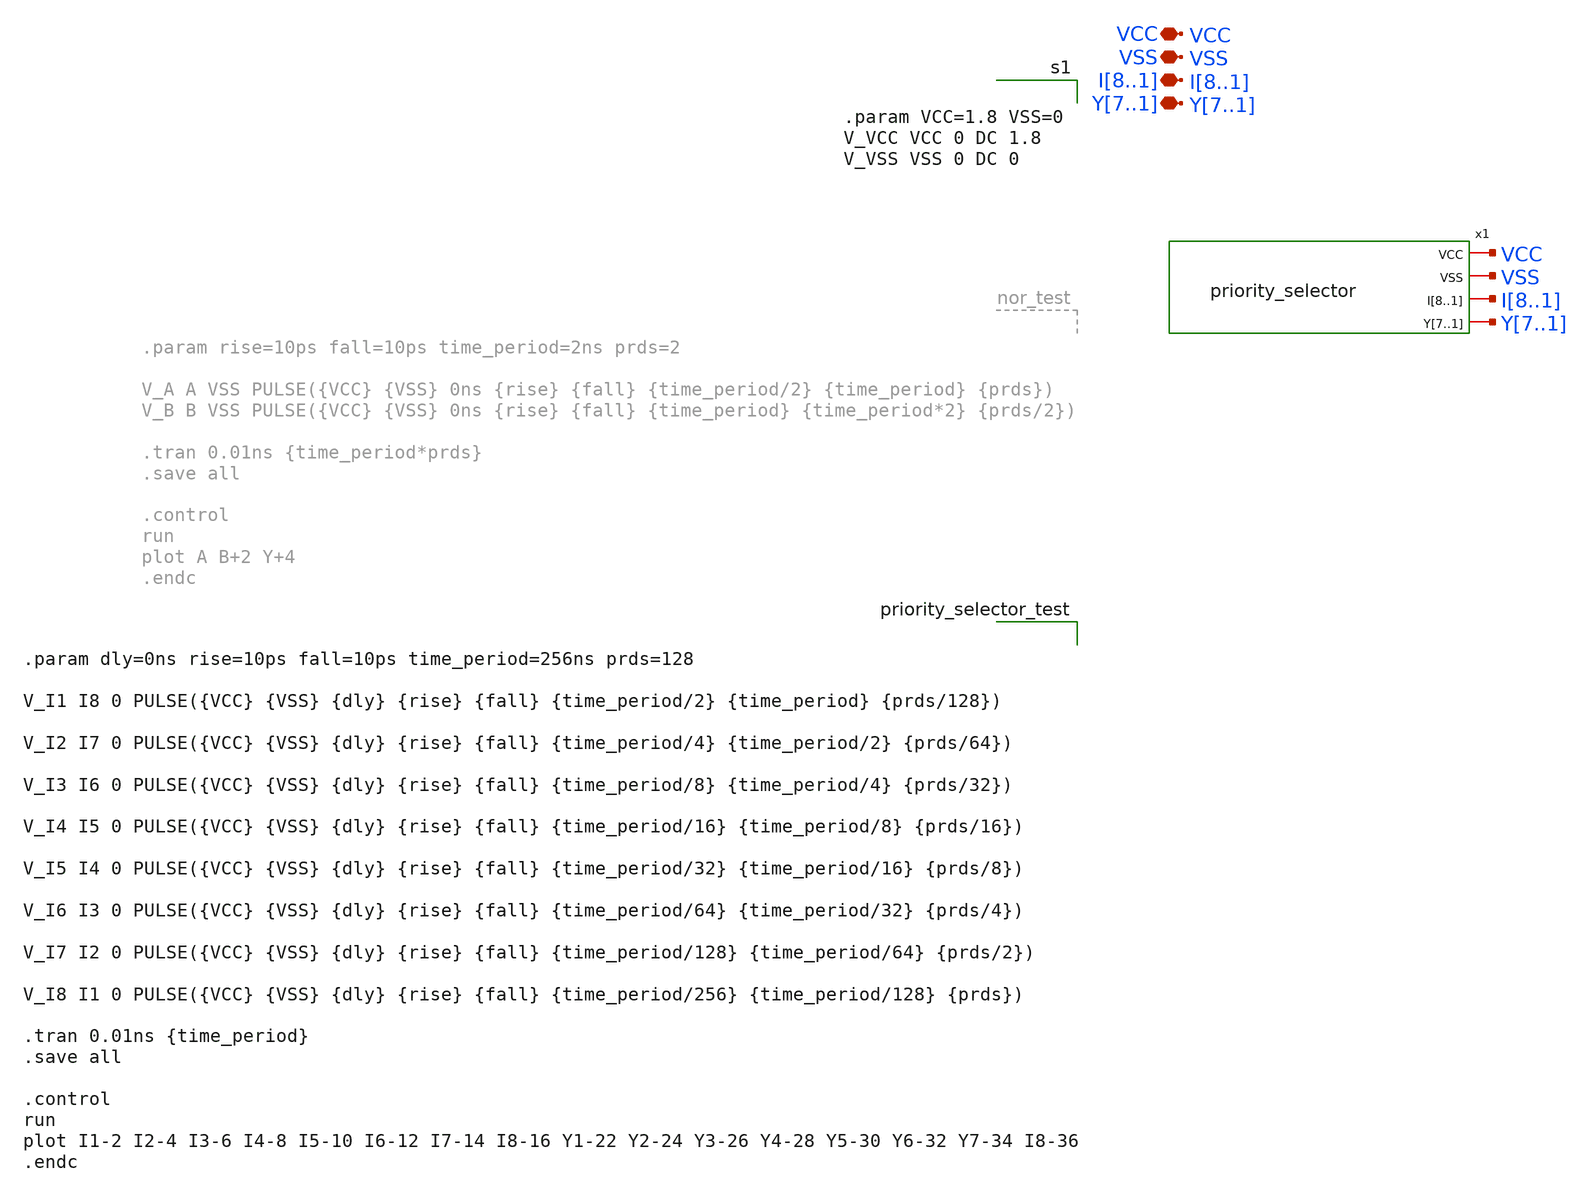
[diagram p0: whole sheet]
** sch_path: peripherals/priority_selector_test.sch
**.subckt priority_selector_test VSS VCC I8,I7,I6,I5,I4,I3,I2,I1 Y7,Y6,Y5,Y4,Y3,Y2,Y1
*.iopin VSS
*.iopin VCC
*.iopin I8,I7,I6,I5,I4,I3,I2,I1
*.iopin Y7,Y6,Y5,Y4,Y3,Y2,Y1
x1 VCC VSS I8 I7 I6 I5 I4 I3 I2 I1 Y7 Y6 Y5 Y4 Y3 Y2 Y1 priority_selector
**** begin user architecture code


.param VCC=1.8 VSS=0
V_VCC VCC 0 DC 1.8
V_VSS VSS 0 DC 0



** opencircuitdesign pdks install
.lib $::SKYWATER_MODELS/sky130.lib.spice tt



.param dly=0ns rise=10ps fall=10ps time_period=256ns prds=128

V_I1 I8 0 PULSE({VCC} {VSS} {dly} {rise} {fall} {time_period/2} {time_period} {prds/128})

V_I2 I7 0 PULSE({VCC} {VSS} {dly} {rise} {fall} {time_period/4} {time_period/2} {prds/64})

V_I3 I6 0 PULSE({VCC} {VSS} {dly} {rise} {fall} {time_period/8} {time_period/4} {prds/32})

V_I4 I5 0 PULSE({VCC} {VSS} {dly} {rise} {fall} {time_period/16} {time_period/8} {prds/16})

V_I5 I4 0 PULSE({VCC} {VSS} {dly} {rise} {fall} {time_period/32} {time_period/16} {prds/8})

V_I6 I3 0 PULSE({VCC} {VSS} {dly} {rise} {fall} {time_period/64} {time_period/32} {prds/4})

V_I7 I2 0 PULSE({VCC} {VSS} {dly} {rise} {fall} {time_period/128} {time_period/64} {prds/2})

V_I8 I1 0 PULSE({VCC} {VSS} {dly} {rise} {fall} {time_period/256} {time_period/128} {prds})

.tran 0.01ns {time_period}
.save all

.control
run
plot I1-2 I2-4 I3-6 I4-8 I5-10 I6-12 I7-14 I8-16 Y1-22 Y2-24 Y3-26 Y4-28 Y5-30 Y6-32 Y7-34 I8-36
.endc


**** end user architecture code
**.ends
.end
